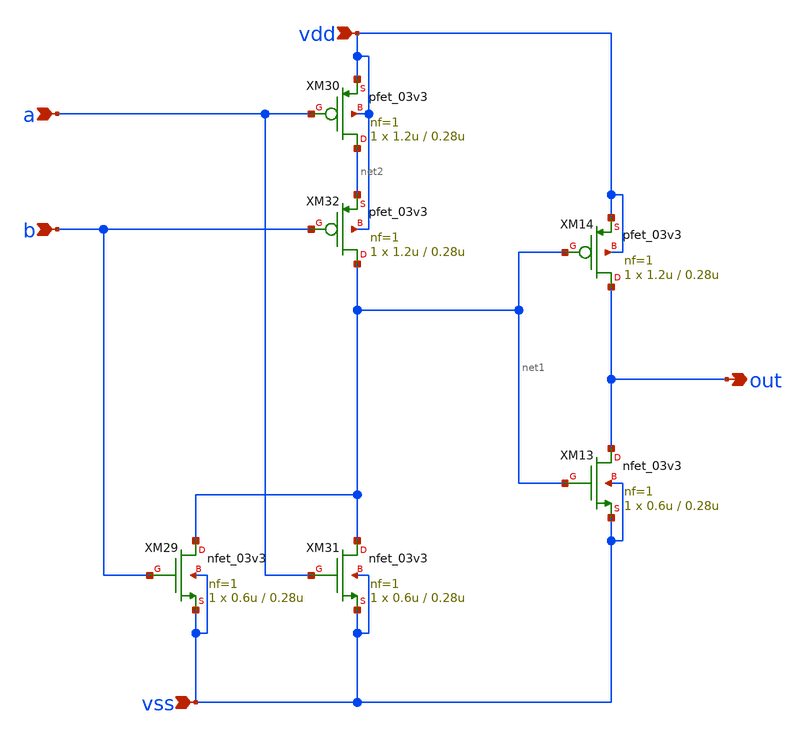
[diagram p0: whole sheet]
** sch_path: xschem/or2.sch
**.subckt or2 a b vdd vss out
*.ipin a
*.ipin b
*.ipin vdd
*.ipin vss
*.opin out
XM29 net1 b vss vss nfet_03v3 L=0.28u W=0.6u nf=1 ad='int((nf+1)/2) * W/nf * 0.18u' as='int((nf+2)/2) * W/nf * 0.18u'
+ pd='2*int((nf+1)/2) * (W/nf + 0.18u)' ps='2*int((nf+2)/2) * (W/nf + 0.18u)' nrd='0.18u / W' nrs='0.18u / W'
+ sa=0 sb=0 sd=0 m=1
XM30 net2 a vdd vdd pfet_03v3 L=0.28u W=1.2u nf=1 ad='int((nf+1)/2) * W/nf * 0.18u' as='int((nf+2)/2) * W/nf * 0.18u'
+ pd='2*int((nf+1)/2) * (W/nf + 0.18u)' ps='2*int((nf+2)/2) * (W/nf + 0.18u)' nrd='0.18u / W' nrs='0.18u / W'
+ sa=0 sb=0 sd=0 m=1
XM31 net1 a vss vss nfet_03v3 L=0.28u W=0.6u nf=1 ad='int((nf+1)/2) * W/nf * 0.18u' as='int((nf+2)/2) * W/nf * 0.18u'
+ pd='2*int((nf+1)/2) * (W/nf + 0.18u)' ps='2*int((nf+2)/2) * (W/nf + 0.18u)' nrd='0.18u / W' nrs='0.18u / W'
+ sa=0 sb=0 sd=0 m=1
XM32 net1 b net2 vdd pfet_03v3 L=0.28u W=1.2u nf=1 ad='int((nf+1)/2) * W/nf * 0.18u' as='int((nf+2)/2) * W/nf * 0.18u'
+ pd='2*int((nf+1)/2) * (W/nf + 0.18u)' ps='2*int((nf+2)/2) * (W/nf + 0.18u)' nrd='0.18u / W' nrs='0.18u / W'
+ sa=0 sb=0 sd=0 m=1
XM13 out net1 vss vss nfet_03v3 L=0.28u W=0.6u nf=1 ad='int((nf+1)/2) * W/nf * 0.18u' as='int((nf+2)/2) * W/nf * 0.18u'
+ pd='2*int((nf+1)/2) * (W/nf + 0.18u)' ps='2*int((nf+2)/2) * (W/nf + 0.18u)' nrd='0.18u / W' nrs='0.18u / W'
+ sa=0 sb=0 sd=0 m=1
XM14 out net1 vdd vdd pfet_03v3 L=0.28u W=1.2u nf=1 ad='int((nf+1)/2) * W/nf * 0.18u' as='int((nf+2)/2) * W/nf * 0.18u'
+ pd='2*int((nf+1)/2) * (W/nf + 0.18u)' ps='2*int((nf+2)/2) * (W/nf + 0.18u)' nrd='0.18u / W' nrs='0.18u / W'
+ sa=0 sb=0 sd=0 m=1
**.ends
.end
